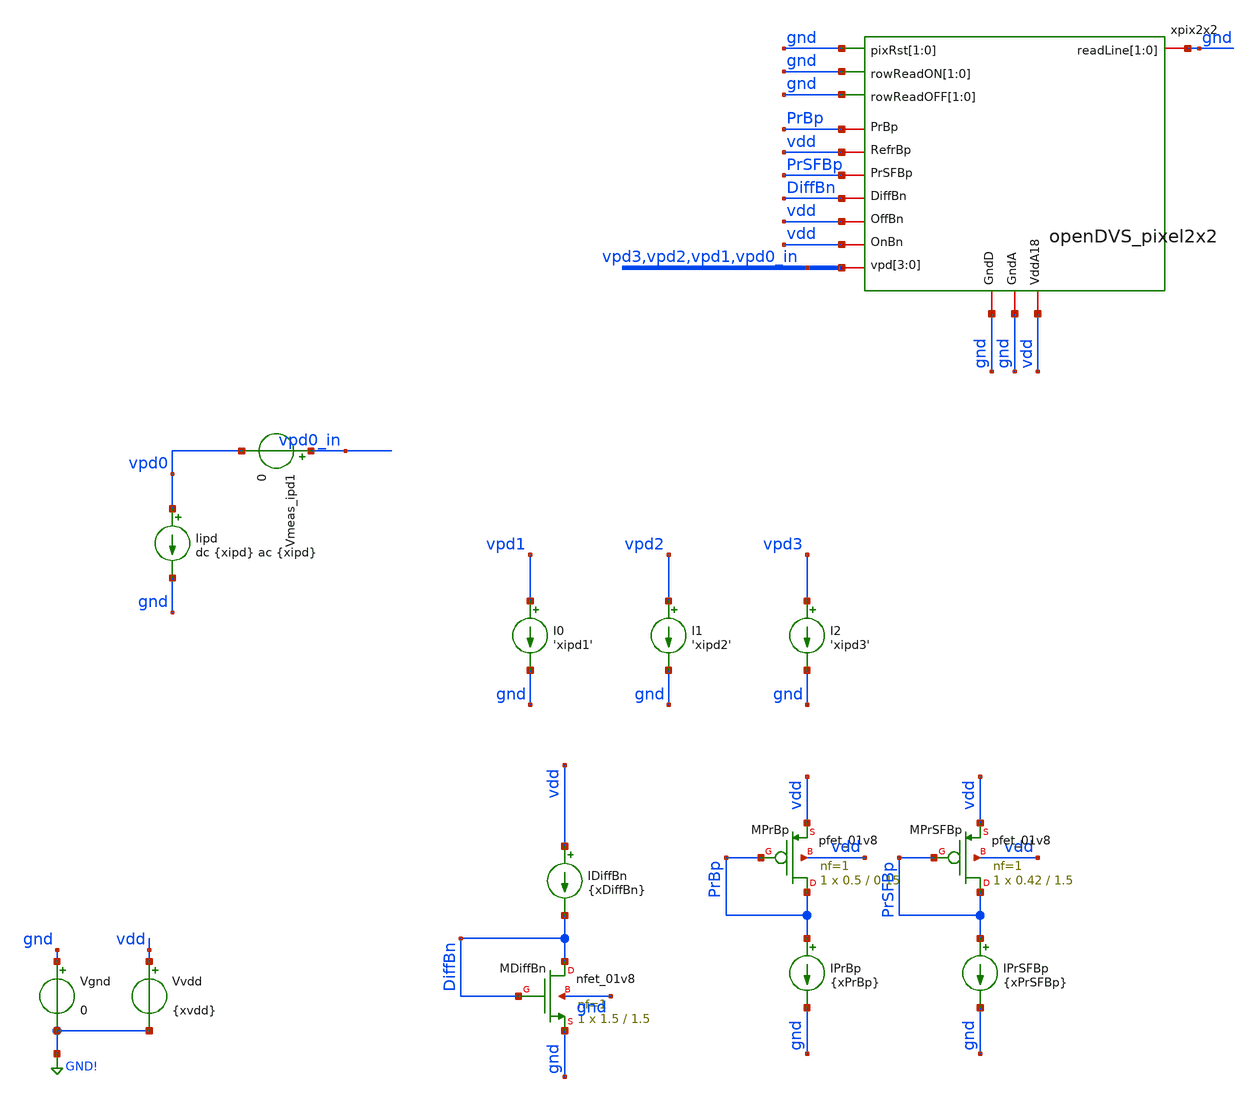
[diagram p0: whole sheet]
** sch_path: analog/klayout/production/final_merge_20260923/testbenches/cace/analog/xschem/tb_PixelGain_ac_2x2.sch
**.subckt tb_PixelGain_ac_2x2
Vgnd gnd GND! 0
Vvdd vdd GND! {xvdd}
Iipd vpd0 gnd dc {xipd} ac {xipd}
Vmeas_ipd1 vpd0_in vpd0 0
XMDiffBn DiffBn DiffBn gnd gnd sky130_fd_pr__nfet_01v8 L=1.5 W=1.5 nf=1 ad='int((1 + 1)/2) * 1.5 / 1 * 0.29'
+ as='int((1 + 2)/2) * 1.5 / 1 * 0.29' pd='2*int((1 + 1)/2) * (1.5 / 1 + 0.29)' ps='2*int((1 + 2)/2) * (1.5 / 1 + 0.29)'
+ nrd='0.29 / 1.5 ' nrs='0.29 / 1.5 ' sa=0 sb=0 sd=0 mult=1 m=1
IDiffBn vdd DiffBn {xDiffBn}
IPrBp PrBp gnd {xPrBp}
XMPrBp PrBp PrBp vdd vdd sky130_fd_pr__pfet_01v8 L=0.15 W=0.5 nf=1 ad='int((1 + 1)/2) * 0.5 / 1 * 0.29'
+ as='int((1 + 2)/2) * 0.5 / 1 * 0.29' pd='2*int((1 + 1)/2) * (0.5 / 1 + 0.29)' ps='2*int((1 + 2)/2) * (0.5 / 1 + 0.29)'
+ nrd='0.29 / 0.5 ' nrs='0.29 / 0.5 ' sa=0 sb=0 sd=0 mult=1 m=1
IPrSFBp PrSFBp gnd {xPrSFBp}
XMPrSFBp PrSFBp PrSFBp vdd vdd sky130_fd_pr__pfet_01v8 L=1.5 W=0.42 nf=1 ad='int((1 + 1)/2) * 0.42 / 1 * 0.29'
+ as='int((1 + 2)/2) * 0.42 / 1 * 0.29' pd='2*int((1 + 1)/2) * (0.42 / 1 + 0.29)' ps='2*int((1 + 2)/2) * (0.42 / 1 + 0.29)'
+ nrd='0.29 / 0.42 ' nrs='0.29 / 0.42 ' sa=0 sb=0 sd=0 mult=1 m=1
xpix2x2 gnd gnd gnd gnd gnd gnd gnd gnd vpd3 vpd2 vpd1 vpd0_in vdd gnd gnd vdd vdd DiffBn PrSFBp vdd
+ PrBp openDVS_pixel2x2
I0 vpd1 gnd 'xipd1'
I1 vpd2 gnd 'xipd2'
I2 vpd3 gnd 'xipd3'
**** begin user architecture code

** opencircuitdesign pdks install
.lib $::SKYWATER_MODELS/sky130.lib.spice tt



.temp 27

.include /home/rpgraca/research/projects/telluride/2025/nic_eventcam/nic2025_openDVS/analog/xschem/openDVS_pixel2x2_pex_simple.spice
*.include /home/rpgraca/research/projects/telluride/2025/nic_eventcam/nic2025_openDVS/analog/xschem/openDVS_pixel2x2_pex_r.spice
*.include /home/rpgraca/research/projects/telluride/2025/nic_eventcam/nic2025_openDVS/analog/xschem/openDVS_pixel2x2_pex_cc.spice
*.include /home/rpgraca/research/projects/telluride/2025/nic_eventcam/nic2025_openDVS/analog/xschem/openDVS_pixel2x2_pex_c.spice
*.include /home/rpgraca/research/projects/telluride/2025/nic_eventcam/nic2025_openDVS/analog/xschem/openDVS_pixel2x2_pex_rcc.spice
*.include /home/rpgraca/research/projects/telluride/2025/nic_eventcam/nic2025_openDVS/analog/xschem/openDVS_pixel2x2_pex_rc.spice



.option gmin=1e-19 abstol=1e-15 vntol=1e-9 reltol=1e-4 chgtol=1e-16
.option itl1=500 itl2=200
.option gminsteps=200 srcsteps=200

.param xipd1 = 1n
.param xipd2 = 1n
.param xipd3 = 1n

.param xvdd = 1.8
.param xipd = 10n
.param xPrBp = 10n
.param xPrSFBp = 10p
.param xDiffBn = 20n
.param xCloadPD = 30f

** nRst at vdd for normal operation (Mrst OFF)
VnRst nRst gnd {xvdd}

** Large inductor: DC short (sets OP) but AC open (no effect on freq response)
** Provides DC path for floating cap node xchamp.vd through vdiff
Lbias xpix2x2.pix[0].vdiff xpix2x2.pix[0].vd 1000T

.save all

.control
** OP with nRst=vdd, .nodeset guides floating nodes
op
write tb_PixelGain_ac_op_2x2.raw

** AC sweep from this operating point
ac dec 50 1m 1G
write tb_PixelGain_ac_2x2.raw

echo
echo '=== AC analysis complete, running post-processing ==='
shell python3
+ /home/rpgraca/research/projects/telluride/2025/nic_eventcam/nic2025_openDVS/analog/xschem/process_PixelGain_ac.py tb_PixelGain_ac_2x2.raw
.endc


**** end user architecture code
**.ends
.GLOBAL GND!
.end
